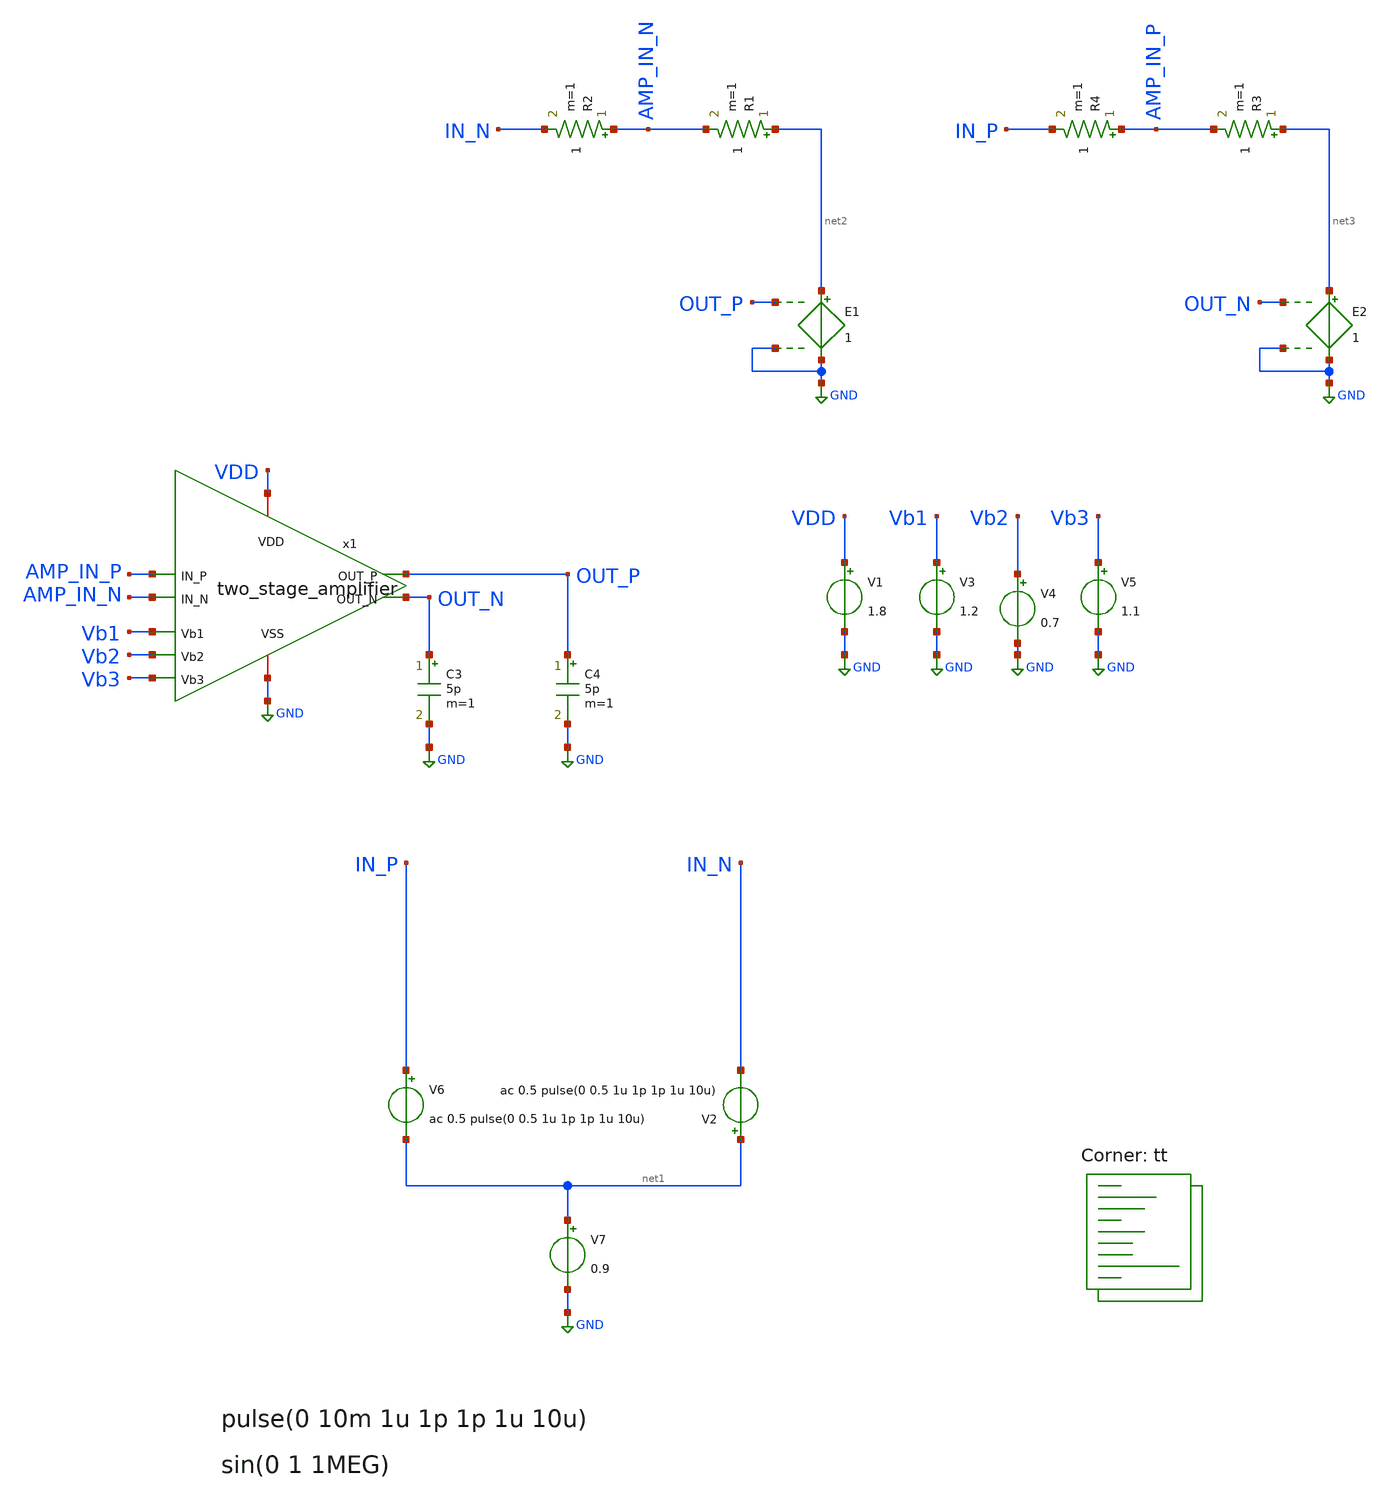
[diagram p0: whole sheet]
** sch_path: xschem/two_stage_amplifier_tran_tb.sch
**.subckt two_stage_amplifier_tran_tb
V1 VDD GND 1.8
.save i(v1)
V3 Vb1 GND 1.2
.save i(v3)
V4 Vb2 GND 0.7
.save i(v4)
V5 Vb3 GND 1.1
.save i(v5)
V6 IN_P net1 ac 0.5 pulse(0 0.5 1u 1p 1p 1u 10u)
.save i(v6)
V7 net1 GND 0.9
.save i(v7)
x1 VDD Vb3 Vb2 Vb1 AMP_IN_P AMP_IN_N OUT_P OUT_N GND two_stage_amplifier
C3 OUT_N GND 5p m=1
C4 OUT_P GND 5p m=1
V2 net1 IN_N ac 0.5 pulse(0 0.5 1u 1p 1p 1u 10u)
.save i(v2)
E1 net2 GND OUT_P GND 1
R1 net2 AMP_IN_N 1 m=1
R2 AMP_IN_N IN_N 1 m=1
E2 net3 GND OUT_N GND 1
R3 net3 AMP_IN_P 1 m=1
R4 AMP_IN_P IN_P 1 m=1
**** begin user architecture code


.temp 25

.param cc=6p
.param rc=38

.control
option savecurrents
option klu
option method=gear
option noacct
option noinit
save all


save @m.x1.xm1.msky130_fd_pr__nfet_01v8_lvt[gm]
save @m.x1.xm1.msky130_fd_pr__nfet_01v8_lvt[id]
save @m.x1.xm1.msky130_fd_pr__nfet_01v8_lvt[vds]

save @m.x1.xm2.msky130_fd_pr__nfet_01v8_lvt[gm]
save @m.x1.xm2.msky130_fd_pr__nfet_01v8_lvt[id]
save @m.x1.xm2.msky130_fd_pr__nfet_01v8_lvt[vds]

save @m.x1.xm3.msky130_fd_pr__nfet_01v8_lvt[gm]
save @m.x1.xm3.msky130_fd_pr__nfet_01v8_lvt[id]
save @m.x1.xm3.msky130_fd_pr__nfet_01v8_lvt[vds]

save @m.x1.xm4.msky130_fd_pr__nfet_01v8_lvt[gm]
save @m.x1.xm4.msky130_fd_pr__nfet_01v8_lvt[id]
save @m.x1.xm4.msky130_fd_pr__nfet_01v8_lvt[vds]

save @m.x1.xm5.msky130_fd_pr__pfet_01v8_lvt[gm]
save @m.x1.xm5.msky130_fd_pr__pfet_01v8_lvt[id]
save @m.x1.xm5.msky130_fd_pr__pfet_01v8_lvt[vds]

save @m.x1.xm6.msky130_fd_pr__pfet_01v8_lvt[gm]
save @m.x1.xm6.msky130_fd_pr__pfet_01v8_lvt[id]
save @m.x1.xm6.msky130_fd_pr__pfet_01v8_lvt[vds]

save @m.x1.xm7.msky130_fd_pr__pfet_01v8_lvt[gm]
save @m.x1.xm7.msky130_fd_pr__pfet_01v8_lvt[id]
save @m.x1.xm7.msky130_fd_pr__pfet_01v8_lvt[vds]

save @m.x1.xm8.msky130_fd_pr__pfet_01v8_lvt[gm]
save @m.x1.xm8.msky130_fd_pr__pfet_01v8_lvt[id]
save @m.x1.xm8.msky130_fd_pr__pfet_01v8_lvt[vds]

save @m.x1.xm9.msky130_fd_pr__nfet_01v8_lvt[gm]
save @m.x1.xm9.msky130_fd_pr__nfet_01v8_lvt[id]
save @m.x1.xm9.msky130_fd_pr__nfet_01v8_lvt[vds]

save @m.x1.xm10.msky130_fd_pr__nfet_01v8_lvt[gm]
save @m.x1.xm10.msky130_fd_pr__nfet_01v8_lvt[id]
save @m.x1.xm10.msky130_fd_pr__nfet_01v8_lvt[vds]

save @m.x1.xm11.msky130_fd_pr__pfet_01v8_lvt[gm]
save @m.x1.xm11.msky130_fd_pr__pfet_01v8_lvt[id]
save @m.x1.xm11.msky130_fd_pr__pfet_01v8_lvt[vds]

save @m.x1.xm12.msky130_fd_pr__pfet_01v8_lvt[gm]
save @m.x1.xm12.msky130_fd_pr__pfet_01v8_lvt[id]
save @m.x1.xm12.msky130_fd_pr__pfet_01v8_lvt[vds]

save @m.x1.xm13.msky130_fd_pr__nfet_01v8_lvt[gm]
save @m.x1.xm13.msky130_fd_pr__nfet_01v8_lvt[id]
save @m.x1.xm13.msky130_fd_pr__nfet_01v8_lvt[vds]

save @m.x1.xm14.msky130_fd_pr__nfet_01v8_lvt[gm]
save @m.x1.xm14.msky130_fd_pr__nfet_01v8_lvt[id]
save @m.x1.xm14.msky130_fd_pr__nfet_01v8_lvt[vds]

op
write two_stage_amplifier_tran_tb.raw


ac dec 10 1k 10G
let out_db = db(mag(out_p - out_n))
let out_ph = phase(out_p - out_n) / pi * 180
plot out_db
plot out_ph
meas ac w_u WHEN out_db=0
meas ac p_x WHEN out_ph=0
meas ac phase_mar find out_ph AT=w_u
let w_u_mhz = w_u / 1e6
print w_u_mhz phase_mar

tran 1n 10u
plot out_p-out_n in_p-in_n

.endc

.lib $::SKYWATER_MODELS/sky130.lib.spice tt
**** end user architecture code
**.ends

* expanding   symbol:  two_stage_amplifier.sym # of pins=9
** sym_path: xschem/two_stage_amplifier.sym
** sch_path: xschem/two_stage_amplifier.sch
.subckt two_stage_amplifier VDD Vb3 Vb2 Vb1 IN_P IN_N OUT_P OUT_N VSS
*.iopin VSS
*.iopin VDD
*.ipin Vb1
*.ipin Vb2
*.ipin Vb3
*.ipin IN_P
*.ipin IN_N
*.opin OUT_N
*.opin OUT_P
XM1 net1 IN_P net3 VSS sky130_fd_pr__nfet_01v8_lvt L=0.3 W=200 nf=1 ad='int((1 + 1)/2) * 200 / 1 * 0.29'
+ as='int((1 + 2)/2) * 200 / 1 * 0.29' pd='2*int((1 + 1)/2) * (200 / 1 + 0.29)' ps='2*int((1 + 2)/2) * (200 / 1 + 0.29)'
+ nrd='0.29 / 200 ' nrs='0.29 / 200 ' sa=0 sb=0 sd=0 mult=4 m=4
XM2 net2 IN_N net3 VSS sky130_fd_pr__nfet_01v8_lvt L=0.3 W=200 nf=1 ad='int((1 + 1)/2) * 200 / 1 * 0.29'
+ as='int((1 + 2)/2) * 200 / 1 * 0.29' pd='2*int((1 + 1)/2) * (200 / 1 + 0.29)' ps='2*int((1 + 2)/2) * (200 / 1 + 0.29)'
+ nrd='0.29 / 200 ' nrs='0.29 / 200 ' sa=0 sb=0 sd=0 mult=4 m=4
XM3 T_OUT_N Vb1 net1 VSS sky130_fd_pr__nfet_01v8_lvt L=0.3 W=200 nf=1 ad='int((1 + 1)/2) * 200 / 1 * 0.29'
+ as='int((1 + 2)/2) * 200 / 1 * 0.29' pd='2*int((1 + 1)/2) * (200 / 1 + 0.29)' ps='2*int((1 + 2)/2) * (200 / 1 + 0.29)'
+ nrd='0.29 / 200 ' nrs='0.29 / 200 ' sa=0 sb=0 sd=0 mult=4 m=4
XM4 T_OUT_P Vb1 net2 VSS sky130_fd_pr__nfet_01v8_lvt L=0.3 W=200 nf=1 ad='int((1 + 1)/2) * 200 / 1 * 0.29'
+ as='int((1 + 2)/2) * 200 / 1 * 0.29' pd='2*int((1 + 1)/2) * (200 / 1 + 0.29)' ps='2*int((1 + 2)/2) * (200 / 1 + 0.29)'
+ nrd='0.29 / 200 ' nrs='0.29 / 200 ' sa=0 sb=0 sd=0 mult=4 m=4
XM5 T_OUT_N Vb2 net4 net4 sky130_fd_pr__pfet_01v8_lvt L=0.8 W=600 nf=1 ad='int((1 + 1)/2) * 600 / 1 * 0.29'
+ as='int((1 + 2)/2) * 600 / 1 * 0.29' pd='2*int((1 + 1)/2) * (600 / 1 + 0.29)' ps='2*int((1 + 2)/2) * (600 / 1 + 0.29)'
+ nrd='0.29 / 600 ' nrs='0.29 / 600 ' sa=0 sb=0 sd=0 mult=1 m=1
XM6 T_OUT_P Vb2 net5 net5 sky130_fd_pr__pfet_01v8_lvt L=0.8 W=600 nf=1 ad='int((1 + 1)/2) * 600 / 1 * 0.29'
+ as='int((1 + 2)/2) * 600 / 1 * 0.29' pd='2*int((1 + 1)/2) * (600 / 1 + 0.29)' ps='2*int((1 + 2)/2) * (600 / 1 + 0.29)'
+ nrd='0.29 / 600 ' nrs='0.29 / 600 ' sa=0 sb=0 sd=0 mult=1 m=1
XM7 net4 Vb3 VDD VDD sky130_fd_pr__pfet_01v8_lvt L=0.8 W=600 nf=1 ad='int((1 + 1)/2) * 600 / 1 * 0.29'
+ as='int((1 + 2)/2) * 600 / 1 * 0.29' pd='2*int((1 + 1)/2) * (600 / 1 + 0.29)' ps='2*int((1 + 2)/2) * (600 / 1 + 0.29)'
+ nrd='0.29 / 600 ' nrs='0.29 / 600 ' sa=0 sb=0 sd=0 mult=1 m=1
XM8 net5 Vb3 VDD VDD sky130_fd_pr__pfet_01v8_lvt L=0.8 W=600 nf=1 ad='int((1 + 1)/2) * 600 / 1 * 0.29'
+ as='int((1 + 2)/2) * 600 / 1 * 0.29' pd='2*int((1 + 1)/2) * (600 / 1 + 0.29)' ps='2*int((1 + 2)/2) * (600 / 1 + 0.29)'
+ nrd='0.29 / 600 ' nrs='0.29 / 600 ' sa=0 sb=0 sd=0 mult=1 m=1
XM9 net3 T_OUT_N VSS VSS sky130_fd_pr__nfet_01v8_lvt L=0.3 W=25 nf=1 ad='int((1 + 1)/2) * 25 / 1 * 0.29'
+ as='int((1 + 2)/2) * 25 / 1 * 0.29' pd='2*int((1 + 1)/2) * (25 / 1 + 0.29)' ps='2*int((1 + 2)/2) * (25 / 1 + 0.29)'
+ nrd='0.29 / 25 ' nrs='0.29 / 25 ' sa=0 sb=0 sd=0 mult=1 m=1
XM10 net3 T_OUT_P VSS VSS sky130_fd_pr__nfet_01v8_lvt L=0.3 W=25 nf=1 ad='int((1 + 1)/2) * 25 / 1 * 0.29'
+ as='int((1 + 2)/2) * 25 / 1 * 0.29' pd='2*int((1 + 1)/2) * (25 / 1 + 0.29)' ps='2*int((1 + 2)/2) * (25 / 1 + 0.29)'
+ nrd='0.29 / 25 ' nrs='0.29 / 25 ' sa=0 sb=0 sd=0 mult=1 m=1
XM12 OUT_N T_OUT_P VDD VDD sky130_fd_pr__pfet_01v8_lvt L=0.35 W=1000 nf=1 ad='int((1 + 1)/2) * 1000 / 1 * 0.29'
+ as='int((1 + 2)/2) * 1000 / 1 * 0.29' pd='2*int((1 + 1)/2) * (1000 / 1 + 0.29)' ps='2*int((1 + 2)/2) * (1000 / 1 + 0.29)'
+ nrd='0.29 / 1000 ' nrs='0.29 / 1000 ' sa=0 sb=0 sd=0 mult=1 m=1
XM11 OUT_P T_OUT_N VDD VDD sky130_fd_pr__pfet_01v8_lvt L=0.35 W=1000 nf=1 ad='int((1 + 1)/2) * 1000 / 1 * 0.29'
+ as='int((1 + 2)/2) * 1000 / 1 * 0.29' pd='2*int((1 + 1)/2) * (1000 / 1 + 0.29)' ps='2*int((1 + 2)/2) * (1000 / 1 + 0.29)'
+ nrd='0.29 / 1000 ' nrs='0.29 / 1000 ' sa=0 sb=0 sd=0 mult=1 m=1
XM14 OUT_N net6 VSS VSS sky130_fd_pr__nfet_01v8_lvt L=0.35 W=500 nf=1 ad='int((1 + 1)/2) * 500 / 1 * 0.29'
+ as='int((1 + 2)/2) * 500 / 1 * 0.29' pd='2*int((1 + 1)/2) * (500 / 1 + 0.29)' ps='2*int((1 + 2)/2) * (500 / 1 + 0.29)'
+ nrd='0.29 / 500 ' nrs='0.29 / 500 ' sa=0 sb=0 sd=0 mult=1 m=1
XM13 OUT_P net6 VSS VSS sky130_fd_pr__nfet_01v8_lvt L=0.35 W=500 nf=1 ad='int((1 + 1)/2) * 500 / 1 * 0.29'
+ as='int((1 + 2)/2) * 500 / 1 * 0.29' pd='2*int((1 + 1)/2) * (500 / 1 + 0.29)' ps='2*int((1 + 2)/2) * (500 / 1 + 0.29)'
+ nrd='0.29 / 500 ' nrs='0.29 / 500 ' sa=0 sb=0 sd=0 mult=1 m=1
R6 OUT_P net6 1e6 m=1
R7 OUT_N net6 1e6 m=1
C1 T_OUT_N net7 {cc} m=1
C2 net8 T_OUT_P {cc} m=1
R9 net7 OUT_P {rc} m=1
R10 net8 OUT_N {rc} m=1
.ends

.GLOBAL GND
.end
